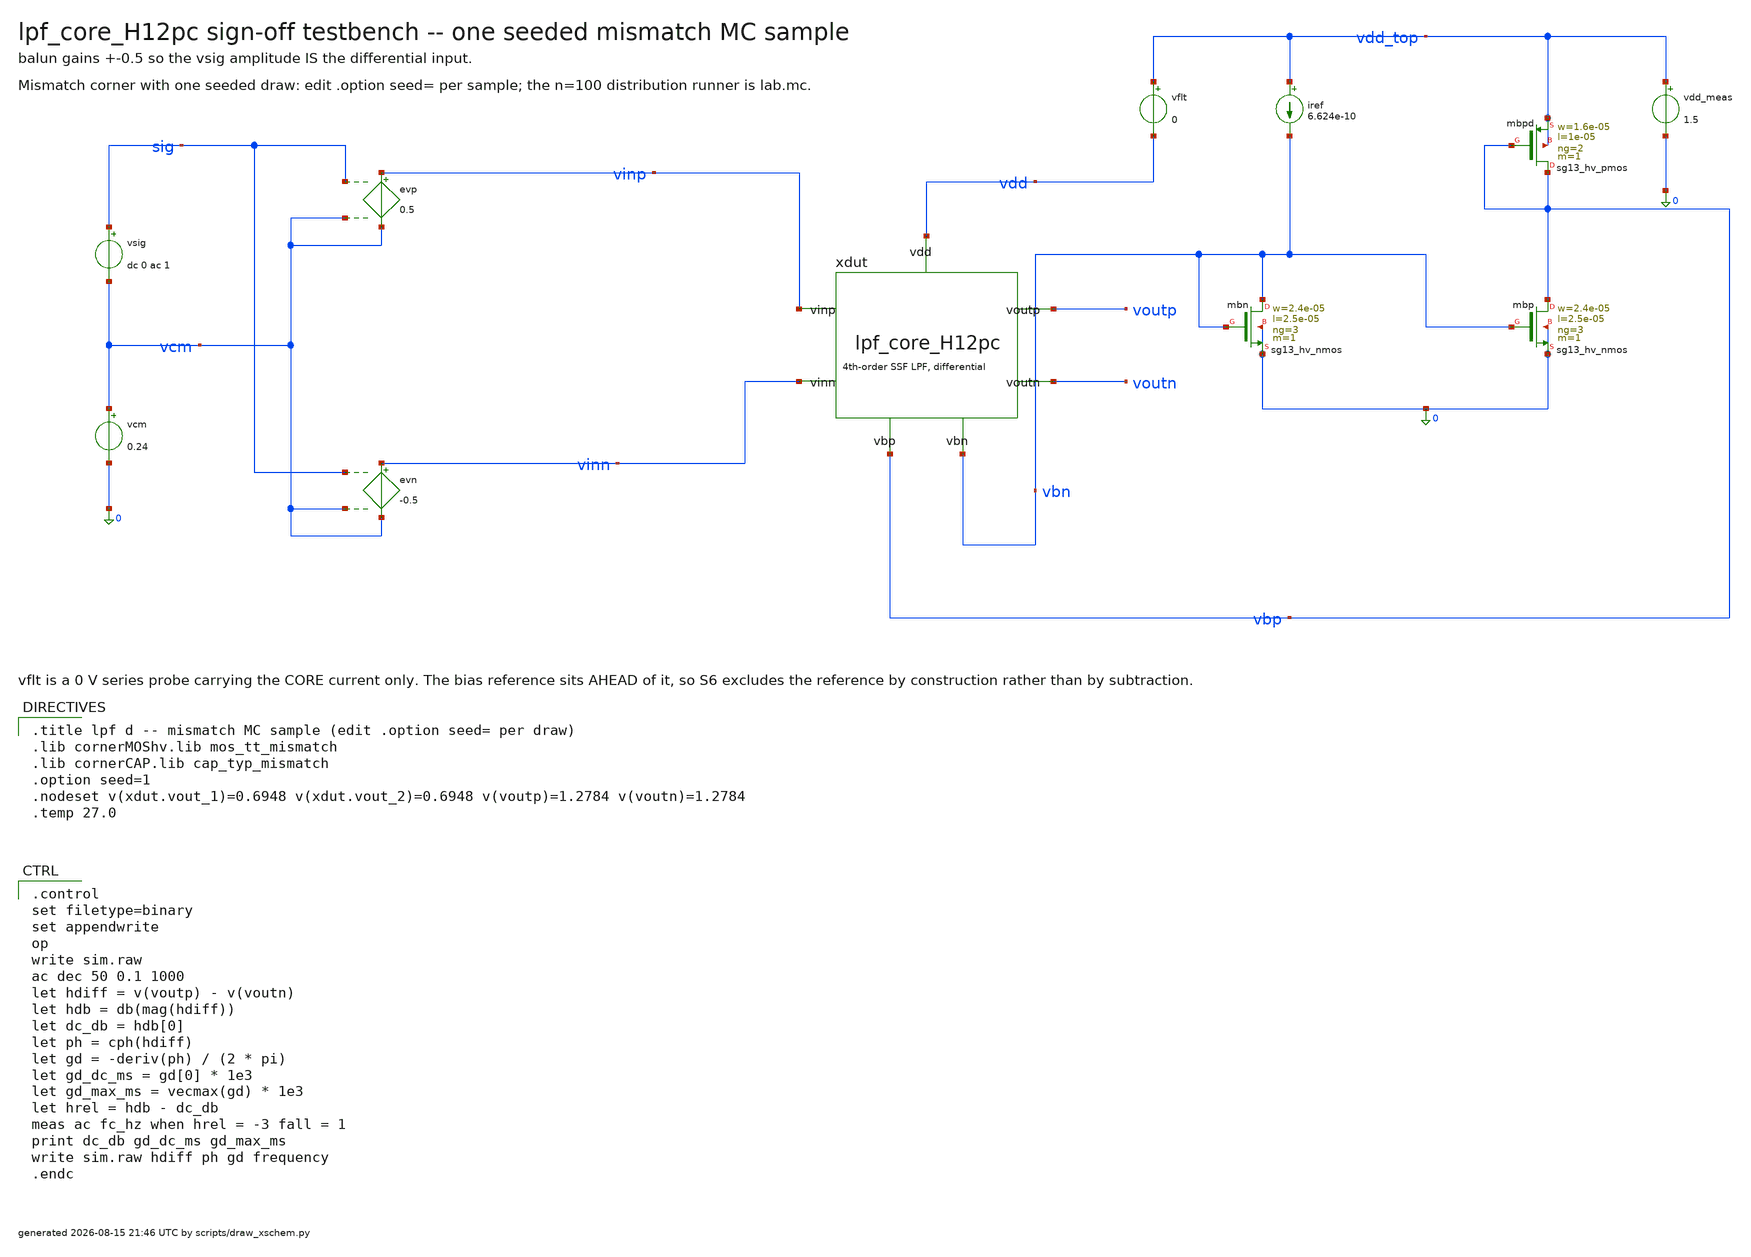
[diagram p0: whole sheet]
** sch_path: signoff/post-pvt/H12-pdk-cap/lpf_tb_H12pc_mc.sch
**.subckt lpf_tb_H12pc_mc
vsig sig vcm dc 0 ac 1
vcm vcm 0 0.24
evp vinp vcm sig vcm 0.5
evn vinn vcm sig vcm -0.5
xdut vinp vinn voutp voutn vbn vbp vdd lpf_core_H12pc
vflt vdd_top vdd 0
vdd_meas vdd_top 0 1.5
iref vdd_top vbn 6.624e-10
Xmbn vbn vbn 0 0 sg13_hv_nmos w=2.4e-05 l=2.5e-05 ng=3 m=1 mm_ok=1
Xmbp vbp vbn 0 0 sg13_hv_nmos w=2.4e-05 l=2.5e-05 ng=3 m=1 mm_ok=1
Xmbpd vbp vbp vdd_top vdd_top sg13_hv_pmos w=1.6e-05 l=1e-05 ng=2 m=1 mm_ok=1
**** begin user architecture code

.title lpf d -- mismatch MC sample (edit .option seed= per draw)
.lib cornerMOShv.lib mos_tt_mismatch
.lib cornerCAP.lib cap_typ_mismatch
.option seed=1
.nodeset v(xdut.vout_1)=0.6948 v(xdut.vout_2)=0.6948 v(voutp)=1.2784 v(voutn)=1.2784
.temp 27.0


.control
set filetype=binary
set appendwrite
op
write sim.raw
ac dec 50 0.1 1000
let hdiff = v(voutp) - v(voutn)
let hdb = db(mag(hdiff))
let dc_db = hdb[0]
let ph = cph(hdiff)
let gd = -deriv(ph) / (2 * pi)
let gd_dc_ms = gd[0] * 1e3
let gd_max_ms = vecmax(gd) * 1e3
let hrel = hdb - dc_db
meas ac fc_hz when hrel = -3 fall = 1
print dc_db gd_dc_ms gd_max_ms
write sim.raw hdiff ph gd frequency
.endc

**** end user architecture code
**.ends

* expanding   symbol:  lpf_core_H12pc.sym # of pins=7
** sym_path: signoff/post-pvt/H12-pdk-cap/lpf_core_H12pc.sym
** sch_path: signoff/post-pvt/H12-pdk-cap/lpf_core_H12pc.sch
.subckt lpf_core_H12pc vinp vinn voutp voutn vbn vbp vdd
*.ipin vinp
*.ipin vinn
*.opin voutp
*.opin voutn
*.ipin vdd
*.ipin vbn
*.ipin vbp
Xm2 net2 vinp vout_1 vout_1 sg13_hv_pmos w=1.6e-05 l=1e-05 ng=2 m=1 mm_ok=1
Xm5 net3 vinn vout_2 vout_2 sg13_hv_pmos w=1.6e-05 l=1e-05 ng=2 m=1 mm_ok=1
Xm4 vout_1 net2 0 0 sg13_hv_nmos w=1.5e-06 l=4.5e-05 ng=1 m=1 mm_ok=1
Xm8 vout_2 net3 0 0 sg13_hv_nmos w=1.5e-06 l=4.5e-05 ng=1 m=1 mm_ok=1
Xm9 net2 vbn 0 0 sg13_hv_nmos w=2.4e-05 l=2.5e-05 ng=3 m=1 mm_ok=1
Xm10 net3 vbn 0 0 sg13_hv_nmos w=2.4e-05 l=2.5e-05 ng=3 m=1 mm_ok=1
Xmst vout_1 vbr net4 net4 sg13_hv_pmos w=5e-06 l=3.3e-05 ng=1 m=1 mm_ok=1
Xmstn vout_2 vbr net1 net1 sg13_hv_pmos w=5e-06 l=3.3e-05 ng=1 m=1 mm_ok=1
Xm0 net4 vout_1 voutp voutp sg13_hv_pmos w=4e-06 l=1.5e-05 ng=1 m=1 mm_ok=1
Xm1 net1 vout_2 voutn voutn sg13_hv_pmos w=4e-06 l=1.5e-05 ng=1 m=1 mm_ok=1
Xm14 voutp net4 vdd vdd sg13_hv_pmos w=1.2e-05 l=3.1e-05 ng=2 m=1 mm_ok=1
Xm15 voutn net1 vdd vdd sg13_hv_pmos w=1.2e-05 l=3.1e-05 ng=2 m=1 mm_ok=1
Xr1 rep_x rep_x vdd vdd sg13_hv_pmos w=1.2e-05 l=3.1e-05 ng=2 m=1 mm_ok=1
Xr2 vbr vbr rep_x rep_x sg13_hv_pmos w=5e-06 l=3.3e-05 ng=1 m=1 mm_ok=1
Xr3 vbr vbn 0 0 sg13_hv_nmos w=2.4e-05 l=2.5e-05 ng=3 m=4 mm_ok=1
Xc13 net2 vout_1 cap_cmim w=40.53u l=40.53u m=2 mm_ok=1
Xc17 net3 vout_2 cap_cmim w=40.53u l=40.53u m=2 mm_ok=1
Xc19 vout_2 vout_1 cap_cmim w=49.42u l=49.42u m=8 mm_ok=1
Xc1 voutp net4 cap_cmim w=49.91u l=49.91u m=16 mm_ok=1
Xc10 voutn net1 cap_cmim w=49.91u l=49.91u m=16 mm_ok=1
Xc12 voutn voutp cap_cmim w=48.45u l=48.45u m=7 mm_ok=1
.ends

.end
